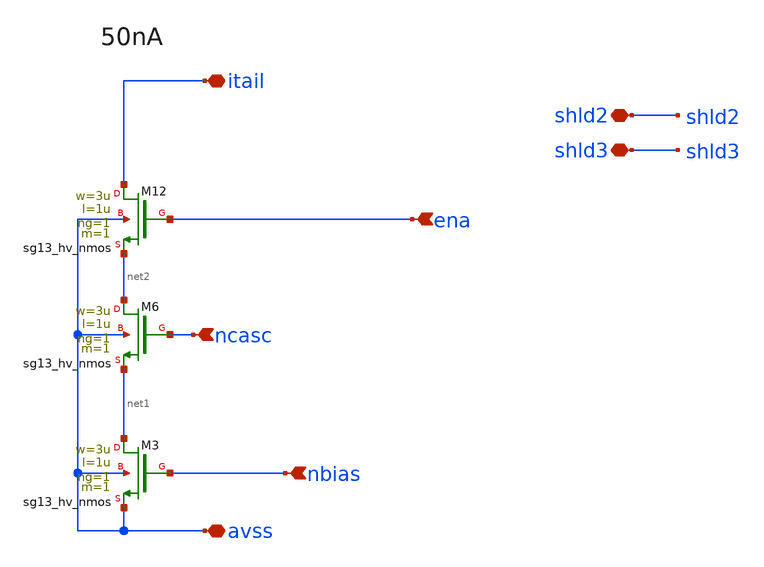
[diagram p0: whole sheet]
** sch_path: xschem/bias_nstack.sch
**.subckt bias_nstack avss ena nbias itail ncasc shld2 shld3
*.iopin avss
*.ipin ena
*.ipin nbias
*.iopin itail
*.ipin ncasc
*.iopin shld2
*.iopin shld3
XM3 net1 nbias avss avss sg13_hv_nmos w=3u l=1u ng=1 m=1 mm_ok=1
XM6 net2 ncasc net1 avss sg13_hv_nmos w=3u l=1u ng=1 m=1 mm_ok=1
XM12 itail ena net2 avss sg13_hv_nmos w=3u l=1u ng=1 m=1 mm_ok=1
**.ends
.end
